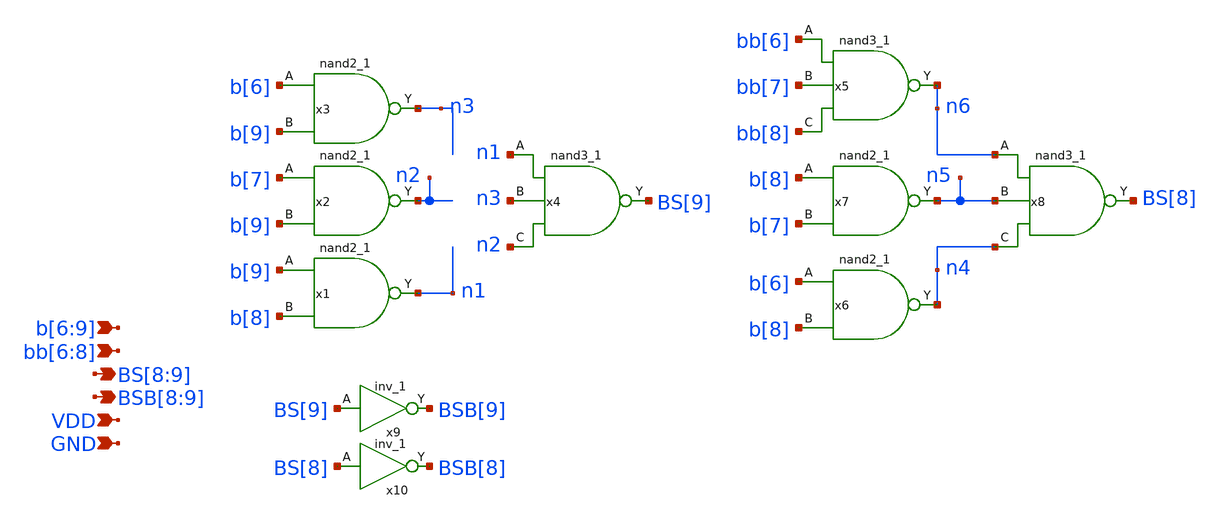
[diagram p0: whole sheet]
** sch_path: xschem/logic_shift_seg2.sch
**.subckt logic_shift_seg2 b[6],b[7],b[8],b[9] BS[8],BS[9] GND VDD bb[6],bb[7],bb[8] BSB[8],BSB[9]
*.ipin b[6],b[7],b[8],b[9]
*.opin BS[8],BS[9]
*.ipin GND
*.ipin VDD
*.ipin bb[6],bb[7],bb[8]
*.opin BSB[8],BSB[9]
x1 b[9] b[8] GND GND VDD VDD n1 sky130_fd_sc_hd__nand2_1
x2 b[7] b[9] GND GND VDD VDD n2 sky130_fd_sc_hd__nand2_1
x3 b[6] b[9] GND GND VDD VDD n3 sky130_fd_sc_hd__nand2_1
x5 bb[6] bb[7] bb[8] GND GND VDD VDD n6 sky130_fd_sc_hd__nand3_1
x4 n1 n3 n2 GND GND VDD VDD BS[9] sky130_fd_sc_hd__nand3_1
x6 b[6] b[8] GND GND VDD VDD n4 sky130_fd_sc_hd__nand2_1
x7 b[8] b[7] GND GND VDD VDD n5 sky130_fd_sc_hd__nand2_1
x8 n6 n5 n4 GND GND VDD VDD BS[8] sky130_fd_sc_hd__nand3_1
x9 BS[9] GND GND VDD VDD BSB[9] sky130_fd_sc_hd__inv_1
x10 BS[8] GND GND VDD VDD BSB[8] sky130_fd_sc_hd__inv_1
**.ends
.end
